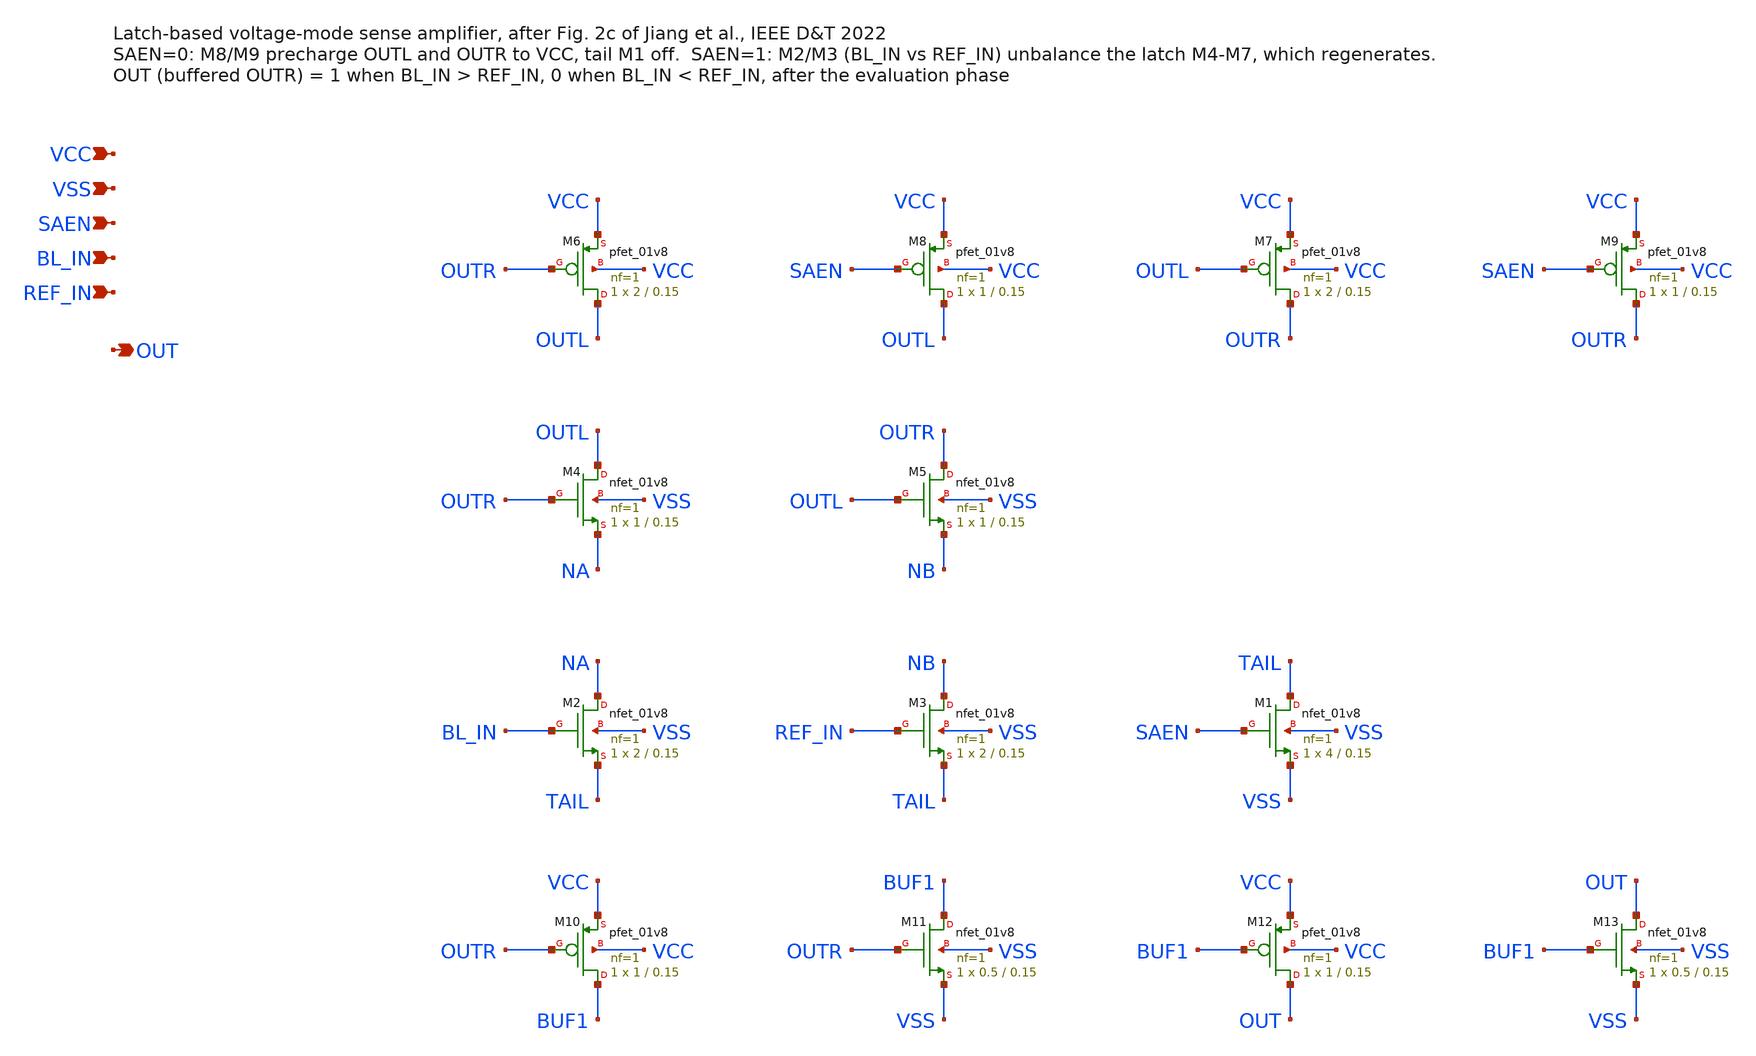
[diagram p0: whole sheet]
** sch_path: CiM components/sense_amp.sch
**.subckt sense_amp VCC VSS SAEN BL_IN REF_IN OUT
*.ipin VCC
*.ipin VSS
*.ipin SAEN
*.ipin BL_IN
*.ipin REF_IN
*.opin OUT
XM6 OUTL OUTR VCC VCC sky130_fd_pr__pfet_01v8 L=0.15 W=2 nf=1 ad='int((nf+1)/2) * W/nf * 0.29' as='int((nf+2)/2) * W/nf * 0.29'
+ pd='2*int((nf+1)/2) * (W/nf + 0.29)' ps='2*int((nf+2)/2) * (W/nf + 0.29)' nrd='0.29 / W' nrs='0.29 / W'
+ sa=0 sb=0 sd=0 mult=1 m=1
XM8 OUTL SAEN VCC VCC sky130_fd_pr__pfet_01v8 L=0.15 W=1 nf=1 ad='int((nf+1)/2) * W/nf * 0.29' as='int((nf+2)/2) * W/nf * 0.29'
+ pd='2*int((nf+1)/2) * (W/nf + 0.29)' ps='2*int((nf+2)/2) * (W/nf + 0.29)' nrd='0.29 / W' nrs='0.29 / W'
+ sa=0 sb=0 sd=0 mult=1 m=1
XM7 OUTR OUTL VCC VCC sky130_fd_pr__pfet_01v8 L=0.15 W=2 nf=1 ad='int((nf+1)/2) * W/nf * 0.29' as='int((nf+2)/2) * W/nf * 0.29'
+ pd='2*int((nf+1)/2) * (W/nf + 0.29)' ps='2*int((nf+2)/2) * (W/nf + 0.29)' nrd='0.29 / W' nrs='0.29 / W'
+ sa=0 sb=0 sd=0 mult=1 m=1
XM9 OUTR SAEN VCC VCC sky130_fd_pr__pfet_01v8 L=0.15 W=1 nf=1 ad='int((nf+1)/2) * W/nf * 0.29' as='int((nf+2)/2) * W/nf * 0.29'
+ pd='2*int((nf+1)/2) * (W/nf + 0.29)' ps='2*int((nf+2)/2) * (W/nf + 0.29)' nrd='0.29 / W' nrs='0.29 / W'
+ sa=0 sb=0 sd=0 mult=1 m=1
XM4 OUTL OUTR NA VSS sky130_fd_pr__nfet_01v8 L=0.15 W=1 nf=1 ad='int((nf+1)/2) * W/nf * 0.29' as='int((nf+2)/2) * W/nf * 0.29'
+ pd='2*int((nf+1)/2) * (W/nf + 0.29)' ps='2*int((nf+2)/2) * (W/nf + 0.29)' nrd='0.29 / W' nrs='0.29 / W'
+ sa=0 sb=0 sd=0 mult=1 m=1
XM5 OUTR OUTL NB VSS sky130_fd_pr__nfet_01v8 L=0.15 W=1 nf=1 ad='int((nf+1)/2) * W/nf * 0.29' as='int((nf+2)/2) * W/nf * 0.29'
+ pd='2*int((nf+1)/2) * (W/nf + 0.29)' ps='2*int((nf+2)/2) * (W/nf + 0.29)' nrd='0.29 / W' nrs='0.29 / W'
+ sa=0 sb=0 sd=0 mult=1 m=1
XM2 NA BL_IN TAIL VSS sky130_fd_pr__nfet_01v8 L=0.15 W=2 nf=1 ad='int((nf+1)/2) * W/nf * 0.29' as='int((nf+2)/2) * W/nf * 0.29'
+ pd='2*int((nf+1)/2) * (W/nf + 0.29)' ps='2*int((nf+2)/2) * (W/nf + 0.29)' nrd='0.29 / W' nrs='0.29 / W'
+ sa=0 sb=0 sd=0 mult=1 m=1
XM3 NB REF_IN TAIL VSS sky130_fd_pr__nfet_01v8 L=0.15 W=2 nf=1 ad='int((nf+1)/2) * W/nf * 0.29' as='int((nf+2)/2) * W/nf * 0.29'
+ pd='2*int((nf+1)/2) * (W/nf + 0.29)' ps='2*int((nf+2)/2) * (W/nf + 0.29)' nrd='0.29 / W' nrs='0.29 / W'
+ sa=0 sb=0 sd=0 mult=1 m=1
XM1 TAIL SAEN VSS VSS sky130_fd_pr__nfet_01v8 L=0.15 W=4 nf=1 ad='int((nf+1)/2) * W/nf * 0.29' as='int((nf+2)/2) * W/nf * 0.29'
+ pd='2*int((nf+1)/2) * (W/nf + 0.29)' ps='2*int((nf+2)/2) * (W/nf + 0.29)' nrd='0.29 / W' nrs='0.29 / W'
+ sa=0 sb=0 sd=0 mult=1 m=1
XM10 BUF1 OUTR VCC VCC sky130_fd_pr__pfet_01v8 L=0.15 W=1 nf=1 ad='int((nf+1)/2) * W/nf * 0.29' as='int((nf+2)/2) * W/nf * 0.29'
+ pd='2*int((nf+1)/2) * (W/nf + 0.29)' ps='2*int((nf+2)/2) * (W/nf + 0.29)' nrd='0.29 / W' nrs='0.29 / W'
+ sa=0 sb=0 sd=0 mult=1 m=1
XM11 BUF1 OUTR VSS VSS sky130_fd_pr__nfet_01v8 L=0.15 W=0.5 nf=1 ad='int((nf+1)/2) * W/nf * 0.29' as='int((nf+2)/2) * W/nf * 0.29'
+ pd='2*int((nf+1)/2) * (W/nf + 0.29)' ps='2*int((nf+2)/2) * (W/nf + 0.29)' nrd='0.29 / W' nrs='0.29 / W'
+ sa=0 sb=0 sd=0 mult=1 m=1
XM12 OUT BUF1 VCC VCC sky130_fd_pr__pfet_01v8 L=0.15 W=1 nf=1 ad='int((nf+1)/2) * W/nf * 0.29' as='int((nf+2)/2) * W/nf * 0.29'
+ pd='2*int((nf+1)/2) * (W/nf + 0.29)' ps='2*int((nf+2)/2) * (W/nf + 0.29)' nrd='0.29 / W' nrs='0.29 / W'
+ sa=0 sb=0 sd=0 mult=1 m=1
XM13 OUT BUF1 VSS VSS sky130_fd_pr__nfet_01v8 L=0.15 W=0.5 nf=1 ad='int((nf+1)/2) * W/nf * 0.29' as='int((nf+2)/2) * W/nf * 0.29'
+ pd='2*int((nf+1)/2) * (W/nf + 0.29)' ps='2*int((nf+2)/2) * (W/nf + 0.29)' nrd='0.29 / W' nrs='0.29 / W'
+ sa=0 sb=0 sd=0 mult=1 m=1
**.ends
.end
